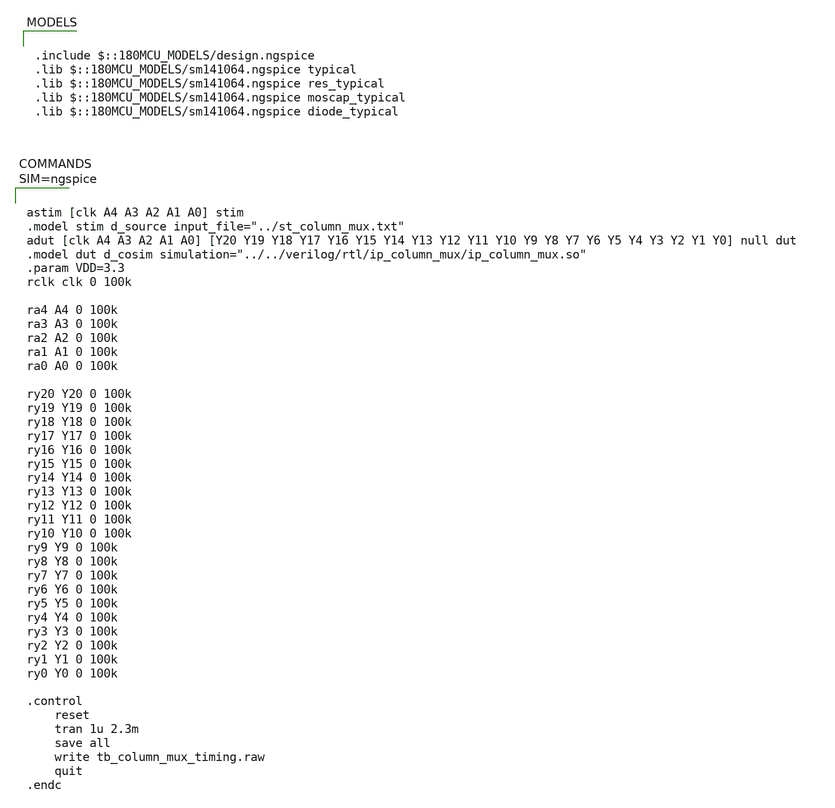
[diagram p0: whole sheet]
** sch_path: xschem/tb_column_mux_timing.sch
**.subckt tb_column_mux_timing
**** begin user architecture code

.include $::180MCU_MODELS/design.ngspice
.lib $::180MCU_MODELS/sm141064.ngspice typical
.lib $::180MCU_MODELS/sm141064.ngspice res_typical
.lib $::180MCU_MODELS/sm141064.ngspice moscap_typical
.lib $::180MCU_MODELS/sm141064.ngspice diode_typical




astim [clk A4 A3 A2 A1 A0] stim
.model stim d_source input_file="../st_column_mux.txt"
adut [clk A4 A3 A2 A1 A0] [Y20 Y19 Y18 Y17 Y16 Y15 Y14 Y13 Y12 Y11 Y10 Y9 Y8 Y7 Y6 Y5 Y4 Y3 Y2 Y1
+ Y0] null dut
.model dut d_cosim simulation="../../verilog/rtl/ip_column_mux/ip_column_mux.so"
.param VDD=3.3
rclk clk 0 100k

ra4 A4 0 100k
ra3 A3 0 100k
ra2 A2 0 100k
ra1 A1 0 100k
ra0 A0 0 100k

ry20 Y20 0 100k
ry19 Y19 0 100k
ry18 Y18 0 100k
ry17 Y17 0 100k
ry16 Y16 0 100k
ry15 Y15 0 100k
ry14 Y14 0 100k
ry13 Y13 0 100k
ry12 Y12 0 100k
ry11 Y11 0 100k
ry10 Y10 0 100k
ry9 Y9 0 100k
ry8 Y8 0 100k
ry7 Y7 0 100k
ry6 Y6 0 100k
ry5 Y5 0 100k
ry4 Y4 0 100k
ry3 Y3 0 100k
ry2 Y2 0 100k
ry1 Y1 0 100k
ry0 Y0 0 100k

.control
	reset
	tran 1u 2.3m
	save all
	write tb_column_mux_timing.raw
	quit
.endc



**** end user architecture code
**.ends
.end
